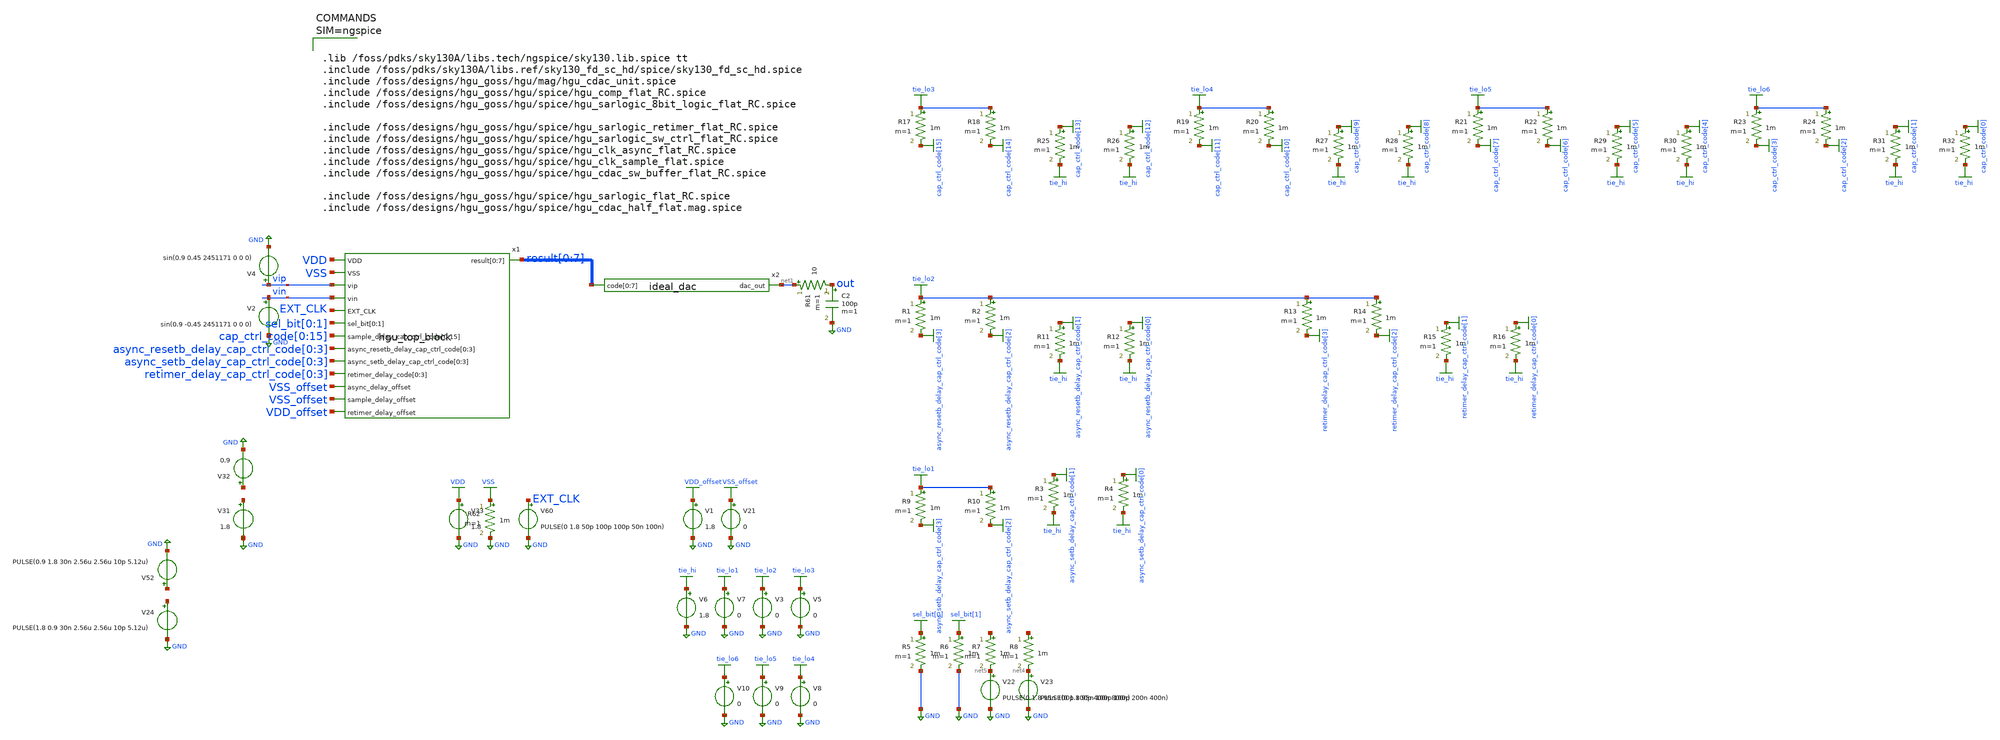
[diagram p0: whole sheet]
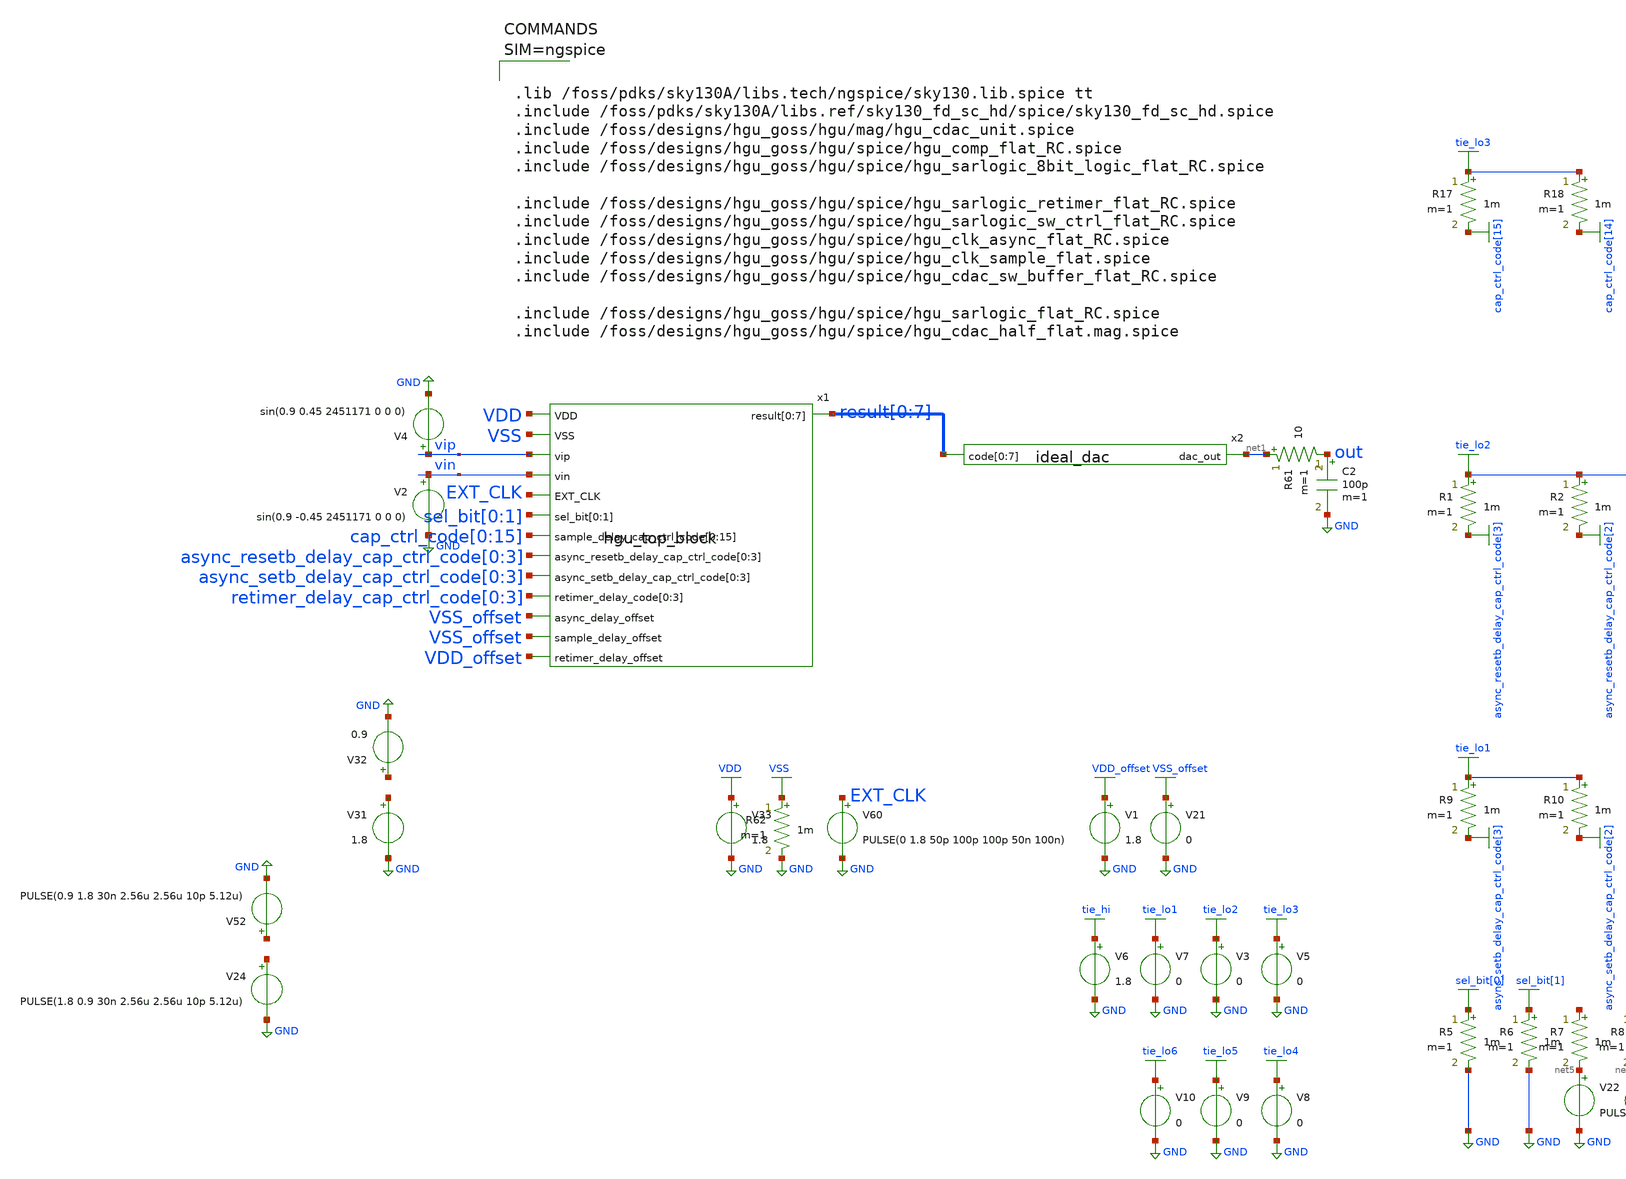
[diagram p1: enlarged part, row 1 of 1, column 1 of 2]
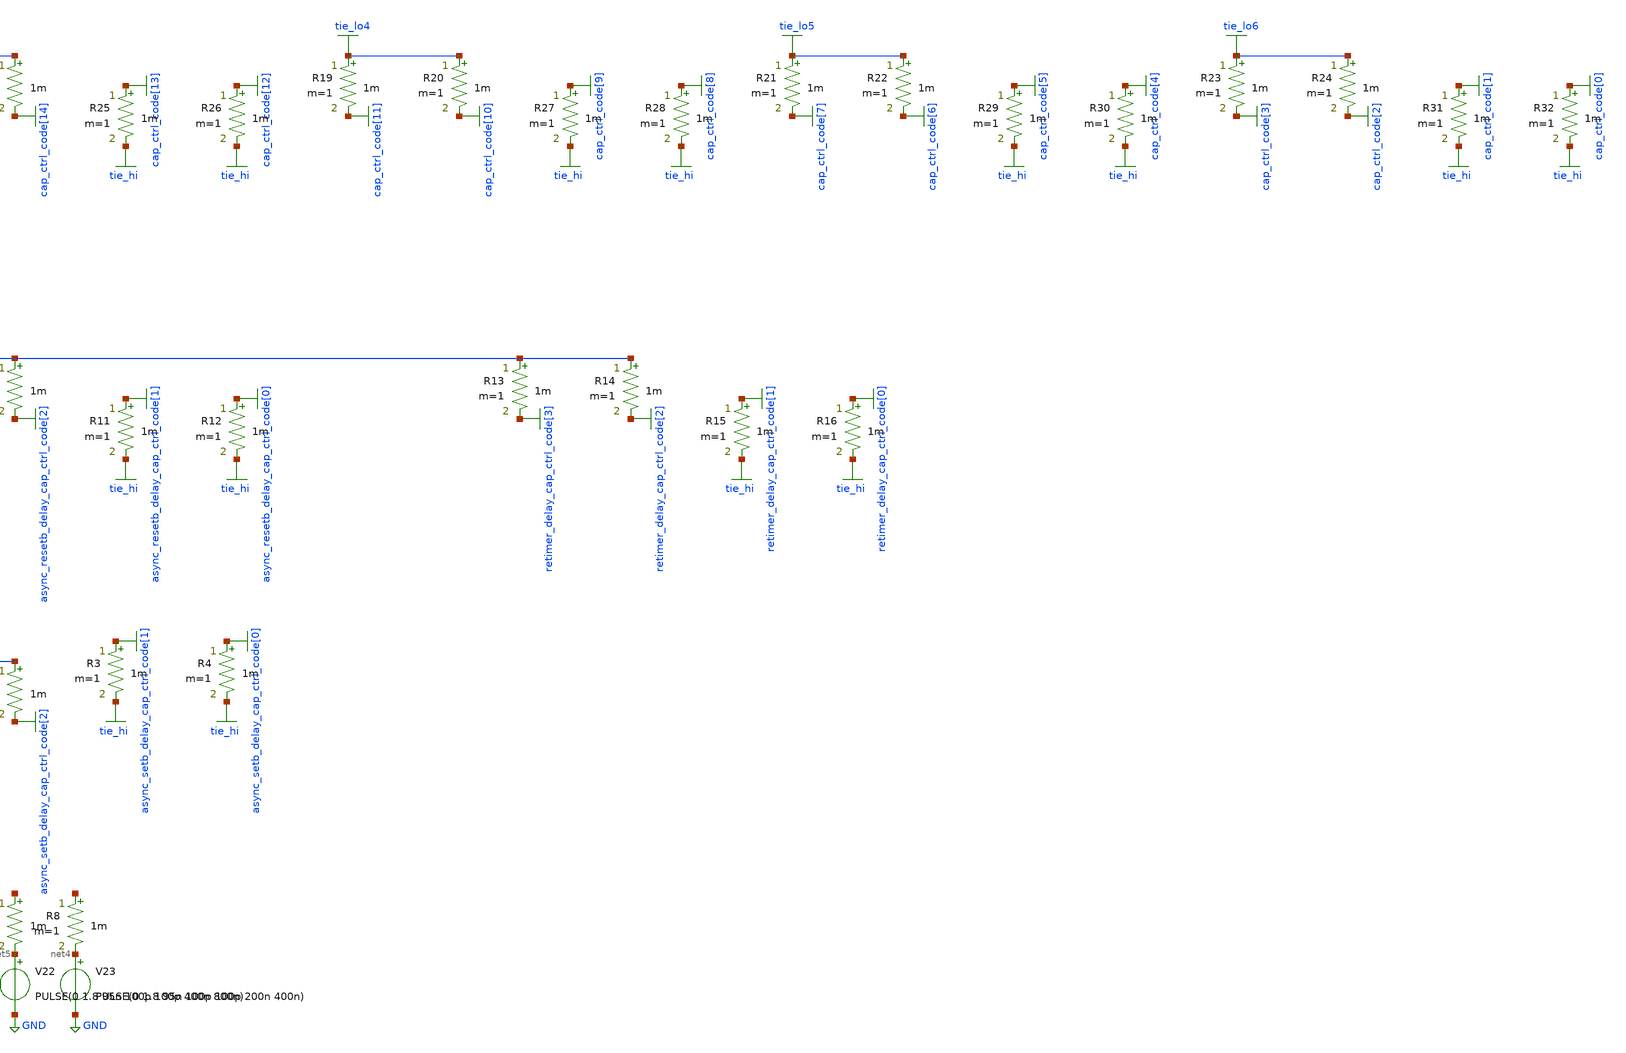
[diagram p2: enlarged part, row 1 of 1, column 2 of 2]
** sch_path: hgu/tb/tb_hgu_top_FFT.sch
**.subckt tb_hgu_top_FFT
x1 VDD result[0] result[1] result[2] result[3] result[4] result[5] result[6] result[7] VSS vip vin
+ EXT_CLK sel_bit[0] sel_bit[1] cap_ctrl_code[0] cap_ctrl_code[1] cap_ctrl_code[2] cap_ctrl_code[3]
+ cap_ctrl_code[4] cap_ctrl_code[5] cap_ctrl_code[6] cap_ctrl_code[7] cap_ctrl_code[8] cap_ctrl_code[9]
+ cap_ctrl_code[10] cap_ctrl_code[11] cap_ctrl_code[12] cap_ctrl_code[13] cap_ctrl_code[14] cap_ctrl_code[15]
+ async_resetb_delay_cap_ctrl_code[0] async_resetb_delay_cap_ctrl_code[1] async_resetb_delay_cap_ctrl_code[2]
+ async_resetb_delay_cap_ctrl_code[3] async_setb_delay_cap_ctrl_code[0] async_setb_delay_cap_ctrl_code[1]
+ async_setb_delay_cap_ctrl_code[2] async_setb_delay_cap_ctrl_code[3] retimer_delay_cap_ctrl_code[0] retimer_delay_cap_ctrl_code[1]
+ retimer_delay_cap_ctrl_code[2] retimer_delay_cap_ctrl_code[3] VSS_offset VSS_offset VDD_offset hgu_top_block
C2 out GND 100p m=1
V33 VDD GND 1.8
V31 net2 GND 1.8
V32 net3 GND 0.9
V60 EXT_CLK GND PULSE(0 1.8 50p 100p 100p 50n 100n)
V2 vin GND sin(0.9 -0.45 2451171 0 0 0)
V4 vip GND sin(0.9 0.45 2451171 0 0 0)
V1 VDD_offset GND 1.8
V21 VSS_offset GND 0
V23 net4 GND PULSE(0 1.8 95n 100p 100p 200n 400n)
V22 net5 GND PULSE(0 1.8 95n 100p 100p 400n 800n)
x2 net1 result[0] result[1] result[2] result[3] result[4] result[5] result[6] result[7] ideal_dac
V24 net6 GND PULSE(1.8 0.9 30n 2.56u 2.56u 10p 5.12u)
V52 net7 GND PULSE(0.9 1.8 30n 2.56u 2.56u 10p 5.12u)
R61 net1 out 10 m=1
R62 VSS GND 1m m=1
R3 async_setb_delay_cap_ctrl_code[1] tie_hi 1m m=1
R4 async_setb_delay_cap_ctrl_code[0] tie_hi 1m m=1
R5 sel_bit[0] GND 1m m=1
R6 sel_bit[1] GND 1m m=1
R7 net8 net5 1m m=1
R8 net9 net4 1m m=1
V6 tie_hi GND 1.8
V7 tie_lo1 GND 0
R9 tie_lo1 async_setb_delay_cap_ctrl_code[3] 1m m=1
R10 tie_lo1 async_setb_delay_cap_ctrl_code[2] 1m m=1
R1 tie_lo2 async_resetb_delay_cap_ctrl_code[3] 1m m=1
R2 tie_lo2 async_resetb_delay_cap_ctrl_code[2] 1m m=1
R11 async_resetb_delay_cap_ctrl_code[1] tie_hi 1m m=1
R12 async_resetb_delay_cap_ctrl_code[0] tie_hi 1m m=1
R13 tie_lo2 retimer_delay_cap_ctrl_code[3] 1m m=1
R14 tie_lo2 retimer_delay_cap_ctrl_code[2] 1m m=1
R15 retimer_delay_cap_ctrl_code[1] tie_hi 1m m=1
R16 retimer_delay_cap_ctrl_code[0] tie_hi 1m m=1
R17 tie_lo3 cap_ctrl_code[15] 1m m=1
R18 tie_lo3 cap_ctrl_code[14] 1m m=1
R19 tie_lo4 cap_ctrl_code[11] 1m m=1
R20 tie_lo4 cap_ctrl_code[10] 1m m=1
R21 tie_lo5 cap_ctrl_code[7] 1m m=1
R22 tie_lo5 cap_ctrl_code[6] 1m m=1
R23 tie_lo6 cap_ctrl_code[3] 1m m=1
R24 tie_lo6 cap_ctrl_code[2] 1m m=1
R25 cap_ctrl_code[13] tie_hi 1m m=1
R26 cap_ctrl_code[12] tie_hi 1m m=1
R27 cap_ctrl_code[9] tie_hi 1m m=1
R28 cap_ctrl_code[8] tie_hi 1m m=1
R29 cap_ctrl_code[5] tie_hi 1m m=1
R30 cap_ctrl_code[4] tie_hi 1m m=1
R31 cap_ctrl_code[1] tie_hi 1m m=1
R32 cap_ctrl_code[0] tie_hi 1m m=1
V3 tie_lo2 GND 0
V5 tie_lo3 GND 0
V8 tie_lo4 GND 0
V9 tie_lo5 GND 0
V10 tie_lo6 GND 0
**** begin user architecture code



.OPTIONS savecurrents
.tran 40ps 500ns
.save vip vin out "result[0] "result[1] "result[2] "result[3] "result[4] "result[5] "result[6] "result[7]
.control
	run
	plot V("result[0]")-4 V("result[1]")-2 V("result[2]") V("result[3]")+2 V("result[4]")+4
+ V("result[5]")+6 V("result[6]")+8 V("result[7]")+10
	plot V(vip) V(vin) V(out)
	setplot tran1
	linearize V(out)
	set specwindow=hanning
	fft V(out)

	plot mag(V(out))
	plot db(V(out))

	*plot V(x1.sample_clk) V(vip) V(vin) V(vip)-V(vin)+0.9 V(x1.tah_vp) V(x1.tah_vn)
+ V(x1.tah_vp)-V(x1.tah_vn)
	*plot V("result[0]")-4 V("result[1]")-2 V("result[2]") V("result[3]")+2 V("result[4]")+4
+ V("result[5]")+6 V("result[6]")+8 V("result[7]")+10
.endc





.lib /foss/pdks/sky130A/libs.tech/ngspice/sky130.lib.spice tt
.include /foss/pdks/sky130A/libs.ref/sky130_fd_sc_hd/spice/sky130_fd_sc_hd.spice
.include /foss/designs/hgu_goss/hgu/mag/hgu_cdac_unit.spice
.include /foss/designs/hgu_goss/hgu/spice/hgu_comp_flat_RC.spice
.include /foss/designs/hgu_goss/hgu/spice/hgu_sarlogic_8bit_logic_flat_RC.spice

.include /foss/designs/hgu_goss/hgu/spice/hgu_sarlogic_retimer_flat_RC.spice
.include /foss/designs/hgu_goss/hgu/spice/hgu_sarlogic_sw_ctrl_flat_RC.spice
.include /foss/designs/hgu_goss/hgu/spice/hgu_clk_async_flat_RC.spice
.include /foss/designs/hgu_goss/hgu/spice/hgu_clk_sample_flat.spice
.include /foss/designs/hgu_goss/hgu/spice/hgu_cdac_sw_buffer_flat_RC.spice

.include /foss/designs/hgu_goss/hgu/spice/hgu_sarlogic_flat_RC.spice
.include /foss/designs/hgu_goss/hgu/spice/hgu_cdac_half_flat.mag.spice



**** end user architecture code
**.ends
.GLOBAL cap_ctrl_code[15]
.GLOBAL cap_ctrl_code[14]
.GLOBAL cap_ctrl_code[13]
.GLOBAL cap_ctrl_code[12]
.GLOBAL cap_ctrl_code[11]
.GLOBAL cap_ctrl_code[10]
.GLOBAL cap_ctrl_code[9]
.GLOBAL cap_ctrl_code[8]
.GLOBAL GND
.GLOBAL async_resetb_delay_cap_ctrl_code[3]
.GLOBAL async_resetb_delay_cap_ctrl_code[2]
.GLOBAL async_resetb_delay_cap_ctrl_code[1]
.GLOBAL async_resetb_delay_cap_ctrl_code[0]
.GLOBAL async_setb_delay_cap_ctrl_code[3]
.GLOBAL async_setb_delay_cap_ctrl_code[2]
.GLOBAL async_setb_delay_cap_ctrl_code[1]
.GLOBAL async_setb_delay_cap_ctrl_code[0]
.GLOBAL cap_ctrl_code[7]
.GLOBAL cap_ctrl_code[6]
.GLOBAL cap_ctrl_code[5]
.GLOBAL cap_ctrl_code[4]
.GLOBAL cap_ctrl_code[3]
.GLOBAL cap_ctrl_code[2]
.GLOBAL cap_ctrl_code[1]
.GLOBAL cap_ctrl_code[0]
.GLOBAL retimer_delay_cap_ctrl_code[3]
.GLOBAL retimer_delay_cap_ctrl_code[2]
.GLOBAL retimer_delay_cap_ctrl_code[1]
.GLOBAL retimer_delay_cap_ctrl_code[0]
.GLOBAL VDD
.GLOBAL VSS
.GLOBAL VDD_offset
.GLOBAL VSS_offset
.GLOBAL sel_bit[1]
.GLOBAL sel_bit[0]
.GLOBAL tie_hi
.GLOBAL tie_lo1
.GLOBAL tie_lo2
.GLOBAL tie_lo3
.GLOBAL tie_lo5
.GLOBAL tie_lo4
.GLOBAL tie_lo6
.end
